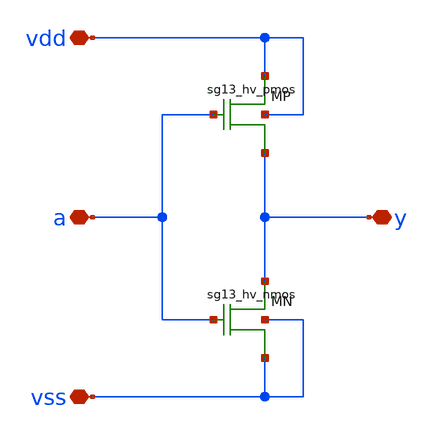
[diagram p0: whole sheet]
** sch_path: xschem/logic_gates/INVHV2T.sch
**.subckt INVHV2T vdd vss y a
*.iopin vdd
*.iopin vss
*.iopin y
*.iopin a
XMP vdd a y vdd sg13_hv_pmos w=6.0u l=0.45u ng=1 m=1
XMN y a vss vss sg13_hv_nmos w=3.0u l=0.45u ng=1 m=1
**.ends
.end
